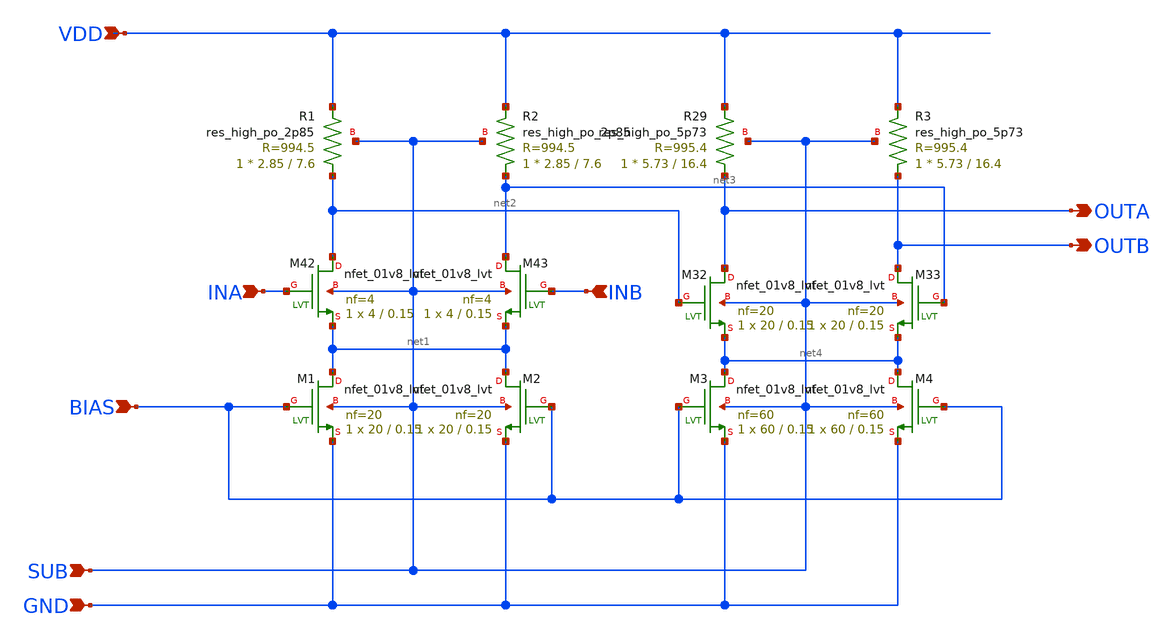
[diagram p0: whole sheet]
** sch_path: xschem/output_buffer.sch
**.subckt output_buffer SUB GND INA BIAS VDD OUTA OUTB INB
*.ipin SUB
*.ipin GND
*.ipin INA
*.ipin BIAS
*.ipin VDD
*.opin OUTA
*.opin OUTB
*.ipin INB
XM42 net2 INA net1 SUB sky130_fd_pr__nfet_01v8_lvt L=0.15 W=4 nf=4 ad='int((nf+1)/2) * W/nf * 0.29' as='int((nf+2)/2) * W/nf * 0.29'
+ pd='2*int((nf+1)/2) * (W/nf + 0.29)' ps='2*int((nf+2)/2) * (W/nf + 0.29)' nrd='0.29 / W' nrs='0.29 / W'
+ sa=0 sb=0 sd=0 mult=1 m=1
XM43 net3 INB net1 SUB sky130_fd_pr__nfet_01v8_lvt L=0.15 W=4 nf=4 ad='int((nf+1)/2) * W/nf * 0.29' as='int((nf+2)/2) * W/nf * 0.29'
+ pd='2*int((nf+1)/2) * (W/nf + 0.29)' ps='2*int((nf+2)/2) * (W/nf + 0.29)' nrd='0.29 / W' nrs='0.29 / W'
+ sa=0 sb=0 sd=0 mult=1 m=1
XR1 net2 VDD SUB sky130_fd_pr__res_high_po_2p85 L=7.6 mult=1 m=1
XR2 net3 VDD SUB sky130_fd_pr__res_high_po_2p85 L=7.6 mult=1 m=1
XM32 OUTA net2 net4 SUB sky130_fd_pr__nfet_01v8_lvt L=0.15 W=20 nf=20 ad='int((nf+1)/2) * W/nf * 0.29'
+ as='int((nf+2)/2) * W/nf * 0.29' pd='2*int((nf+1)/2) * (W/nf + 0.29)' ps='2*int((nf+2)/2) * (W/nf + 0.29)'
+ nrd='0.29 / W' nrs='0.29 / W' sa=0 sb=0 sd=0 mult=1 m=1
XM33 OUTB net3 net4 SUB sky130_fd_pr__nfet_01v8_lvt L=0.15 W=20 nf=20 ad='int((nf+1)/2) * W/nf * 0.29'
+ as='int((nf+2)/2) * W/nf * 0.29' pd='2*int((nf+1)/2) * (W/nf + 0.29)' ps='2*int((nf+2)/2) * (W/nf + 0.29)'
+ nrd='0.29 / W' nrs='0.29 / W' sa=0 sb=0 sd=0 mult=1 m=1
XM1 net1 BIAS GND SUB sky130_fd_pr__nfet_01v8_lvt L=0.15 W=20 nf=20 ad='int((nf+1)/2) * W/nf * 0.29'
+ as='int((nf+2)/2) * W/nf * 0.29' pd='2*int((nf+1)/2) * (W/nf + 0.29)' ps='2*int((nf+2)/2) * (W/nf + 0.29)'
+ nrd='0.29 / W' nrs='0.29 / W' sa=0 sb=0 sd=0 mult=1 m=1
XM2 net1 BIAS GND SUB sky130_fd_pr__nfet_01v8_lvt L=0.15 W=20 nf=20 ad='int((nf+1)/2) * W/nf * 0.29'
+ as='int((nf+2)/2) * W/nf * 0.29' pd='2*int((nf+1)/2) * (W/nf + 0.29)' ps='2*int((nf+2)/2) * (W/nf + 0.29)'
+ nrd='0.29 / W' nrs='0.29 / W' sa=0 sb=0 sd=0 mult=1 m=1
XM3 net4 BIAS GND SUB sky130_fd_pr__nfet_01v8_lvt L=0.15 W=60 nf=60 ad='int((nf+1)/2) * W/nf * 0.29'
+ as='int((nf+2)/2) * W/nf * 0.29' pd='2*int((nf+1)/2) * (W/nf + 0.29)' ps='2*int((nf+2)/2) * (W/nf + 0.29)'
+ nrd='0.29 / W' nrs='0.29 / W' sa=0 sb=0 sd=0 mult=1 m=1
XM4 net4 BIAS GND SUB sky130_fd_pr__nfet_01v8_lvt L=0.15 W=60 nf=60 ad='int((nf+1)/2) * W/nf * 0.29'
+ as='int((nf+2)/2) * W/nf * 0.29' pd='2*int((nf+1)/2) * (W/nf + 0.29)' ps='2*int((nf+2)/2) * (W/nf + 0.29)'
+ nrd='0.29 / W' nrs='0.29 / W' sa=0 sb=0 sd=0 mult=1 m=1
XR29 OUTA VDD SUB sky130_fd_pr__res_high_po_5p73 L=16.4 mult=1 m=1
XR3 OUTB VDD SUB sky130_fd_pr__res_high_po_5p73 L=16.4 mult=1 m=1
**.ends
.end
